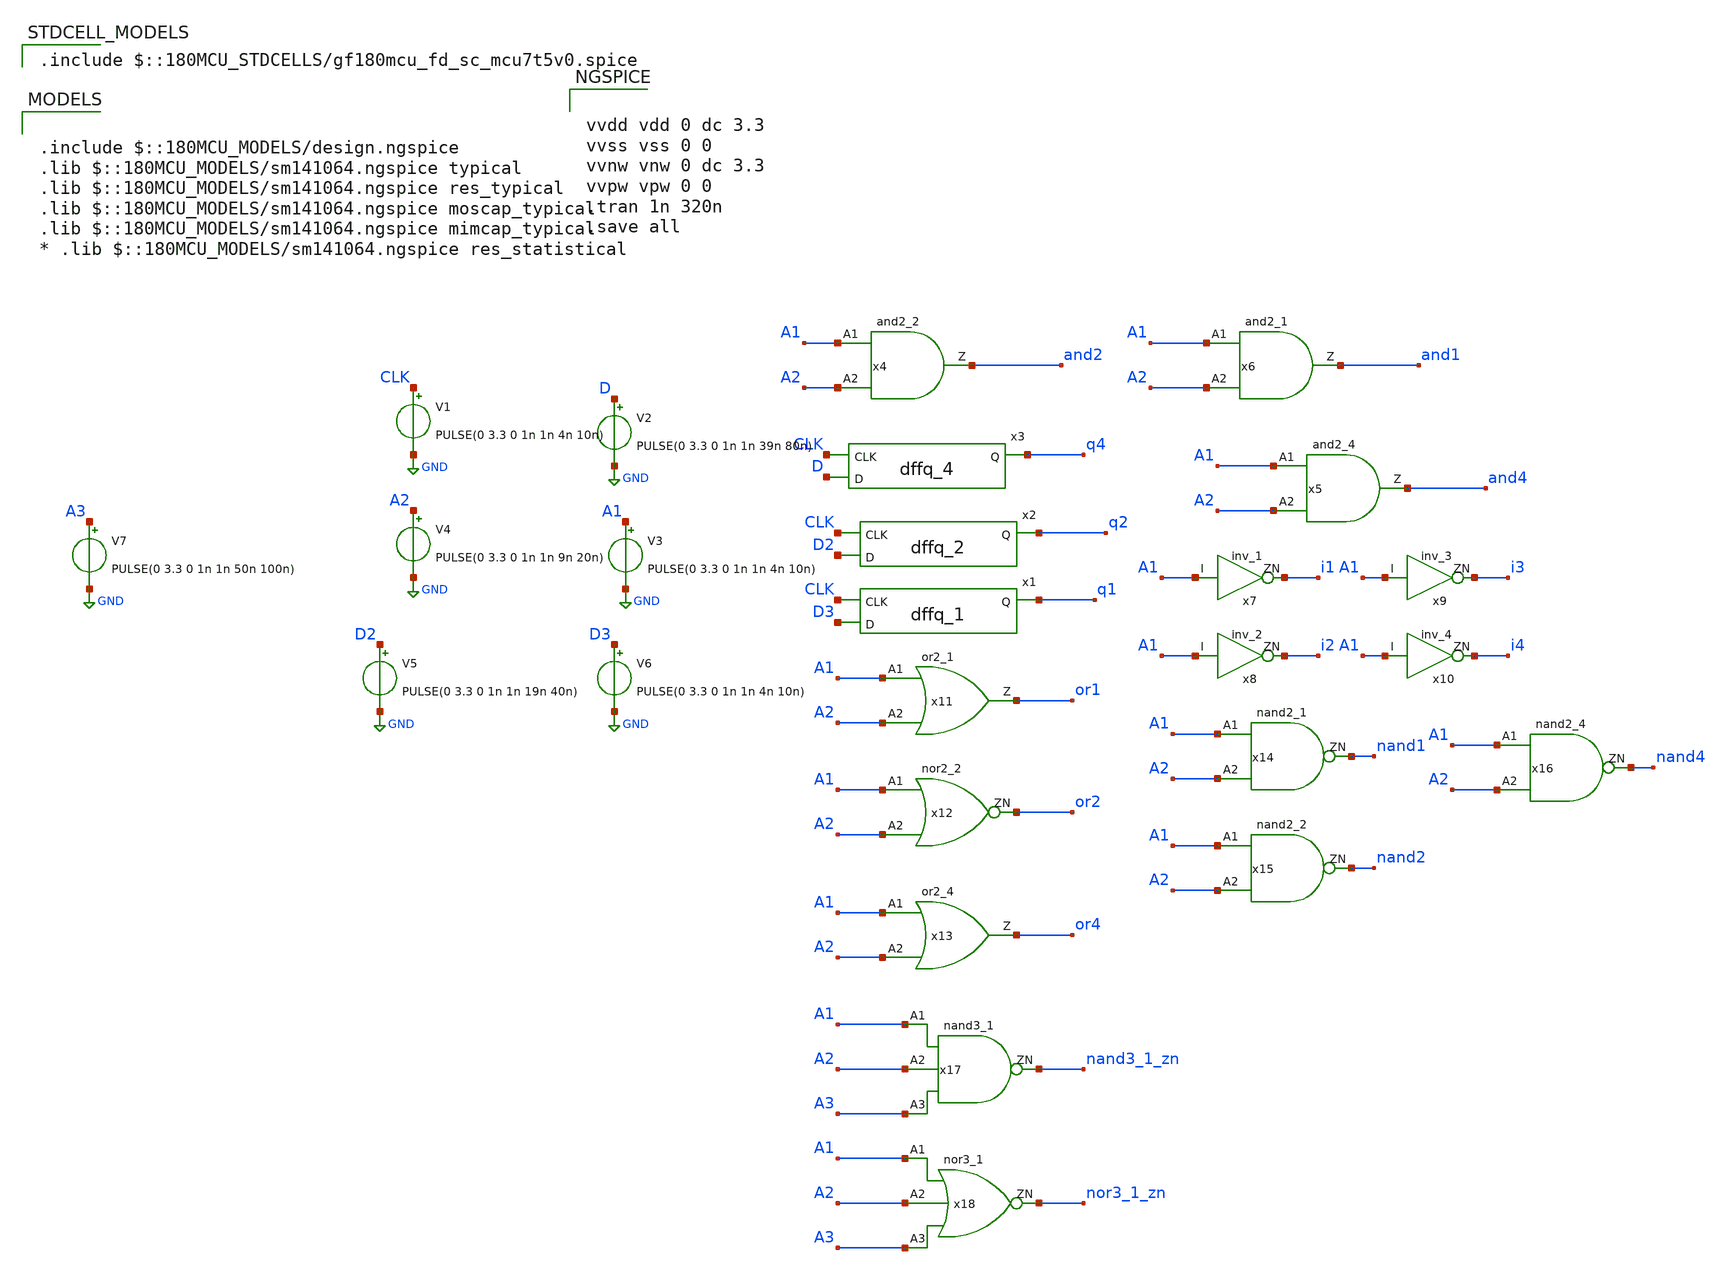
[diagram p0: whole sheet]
** sch_path: xschem/test_symbols.sch
**.subckt test_symbols
x1 CLK D3 VDD VNW VPW VSS gf180mcu_fd_sc_mcu7t5v0__dffq_1
x2 D2 CLK q2 VDD VNW VPW VSS gf180mcu_fd_sc_mcu7t5v0__dffq_2
x3 CLK D VDD VNW VPW VSS gf180mcu_fd_sc_mcu7t5v0__dffq_4
V1 CLK GND PULSE(0 3.3 0 1n 1n 4n 10n)
V2 D GND PULSE(0 3.3 0 1n 1n 39n 80n)
x4 A1 A2 and2 VDD VNW VPW VSS gf180mcu_fd_sc_mcu7t5v0__and2_2
V3 A1 GND PULSE(0 3.3 0 1n 1n 4n 10n)
V4 A2 GND PULSE(0 3.3 0 1n 1n 9n 20n)
x6 A1 A2 and1 VDD VNW VPW VSS gf180mcu_fd_sc_mcu7t5v0__and2_1
x5 A1 A2 and4 VDD VNW VPW VSS gf180mcu_fd_sc_mcu7t5v0__and2_4
x7 A1 i1 VDD VNW VPW VSS gf180mcu_fd_sc_mcu7t5v0__inv_1
x8 A1 i2 VDD VNW VPW VSS gf180mcu_fd_sc_mcu7t5v0__inv_2
x9 A1 i3 VDD VNW VPW VSS gf180mcu_fd_sc_mcu7t5v0__inv_3
x10 A1 i4 VDD VNW VPW VSS gf180mcu_fd_sc_mcu7t5v0__inv_4
x11 A1 A2 or1 VDD VNW VPW VSS gf180mcu_fd_sc_mcu7t5v0__or2_1
x12 A1 A2 or2 VDD VPW VSS gf180mcu_fd_sc_mcu7t5v0__nor2_2
x13 A1 A2 or4 VDD VNW VPW VSS gf180mcu_fd_sc_mcu7t5v0__or2_4
x14 A1 A2 nand1 VDD VNW VPW VSS gf180mcu_fd_sc_mcu7t5v0__nand2_1
x15 A1 A2 nand2 VDD VNW VPW VSS gf180mcu_fd_sc_mcu7t5v0__nand2_2
x16 A1 A2 nand4 VDD VNW VPW VSS gf180mcu_fd_sc_mcu7t5v0__nand2_4
V5 D2 GND PULSE(0 3.3 0 1n 1n 19n 40n)
V6 D3 GND PULSE(0 3.3 0 1n 1n 4n 10n)
x17 A1 A2 A3 nand3_1_zn VDD VNW VPW VSS gf180mcu_fd_sc_mcu7t5v0__nand3_1
x18 A1 A2 A3 nor3_1_zn VDD VNW VPW VSS gf180mcu_fd_sc_mcu7t5v0__nor3_1
V7 A3 GND PULSE(0 3.3 0 1n 1n 50n 100n)
**** begin user architecture code


vvdd vdd 0 dc 3.3
vvss vss 0 0
vvnw vnw 0 dc 3.3
vvpw vpw 0 0
.tran 1n 320n
.save all



.include $::180MCU_MODELS/design.ngspice
.lib $::180MCU_MODELS/sm141064.ngspice typical
.lib $::180MCU_MODELS/sm141064.ngspice res_typical
.lib $::180MCU_MODELS/sm141064.ngspice moscap_typical
.lib $::180MCU_MODELS/sm141064.ngspice mimcap_typical
* .lib $::180MCU_MODELS/sm141064.ngspice res_statistical

 .include $::180MCU_STDCELLS/gf180mcu_fd_sc_mcu7t5v0.spice
**** end user architecture code
**.ends
.GLOBAL GND
.end
